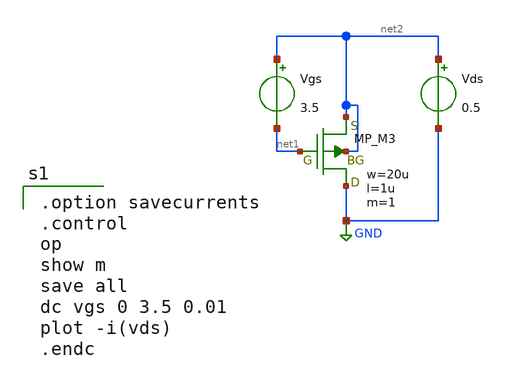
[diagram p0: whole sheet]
** sch_path: member_project/DCDC/xschem/pmos_id.sch
**.subckt pmos_id
XM3 GND net1 net2 net2 PMOS w=20u l=1u as=0 ad=0 ps=0 pd=0 nrd=0 nrs=0 m=1
Vgs net2 net1 3.5
Vds net2 GND 0.5
**** begin user architecture code
 .include $::LIB/ip62_models

.option savecurrents
.control
op
show m
save all
dc vgs 0 3.5 0.01
plot -i(vds)
.endc

**** end user architecture code
**.ends
.GLOBAL GND
.end
